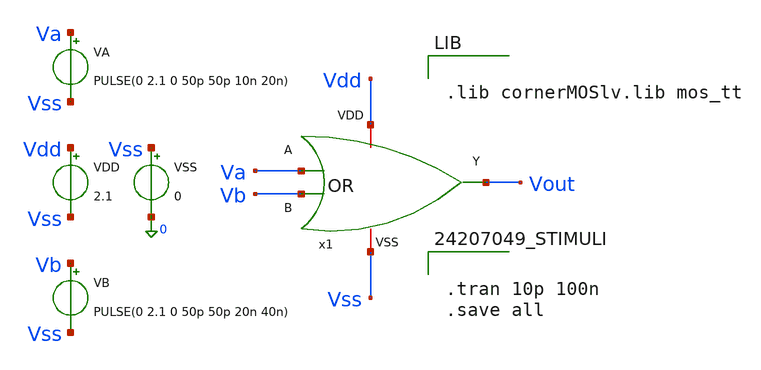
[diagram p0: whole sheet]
** sch_path: logic_gate/OR2/PRE-SIMULATION/OR_test.sch
**.subckt OR_test
VDD Vdd Vss 2.1
VSS Vss 0 0
VA Va Vss PULSE(0 2.1 0 50p 50p 10n 20n)
VB Vb Vss PULSE(0 2.1 0 50p 50p 20n 40n)
x1 Vdd Va Vb Vout Vss OR
**** begin user architecture code


.tran 10p 100n
.save all




.lib cornerMOSlv.lib mos_tt


**** end user architecture code
**.ends

* expanding   symbol:  /home/tundzi-lp1710/LAYOUT_ANALOG_FALL_DTVT/Bai_Tap_Buoi_2/OR_GATE/OR.sym #
*+ of pins=5
** sym_path: logic_gate/OR2/PRE-SIMULATION/OR.sym
** sch_path: logic_gate/OR2/PRE-SIMULATION/OR.sch
.subckt OR VDD A B Y VSS
*.ipin A
*.ipin B
*.opin Y
*.iopin VDD
*.iopin VSS
XM1 net2 A VSS VSS sg13_lv_nmos w=0.15u l=0.13u ng=1 m=1 mm_ok=1
XM2 net1 A VDD VDD sg13_lv_pmos w=0.15u l=0.13u ng=1 m=1 mm_ok=1
XM3 net2 B net1 VDD sg13_lv_pmos w=0.15u l=0.13u ng=1 m=1 mm_ok=1
XM4 net2 B VSS VSS sg13_lv_nmos w=0.15u l=0.13u ng=1 m=1 mm_ok=1
XM5 Y net2 VDD VDD sg13_lv_pmos w=0.15u l=0.13u ng=1 m=1 mm_ok=1
XM6 Y net2 VSS VSS sg13_lv_nmos w=0.15u l=0.13u ng=1 m=1 mm_ok=1
.ends

.end
